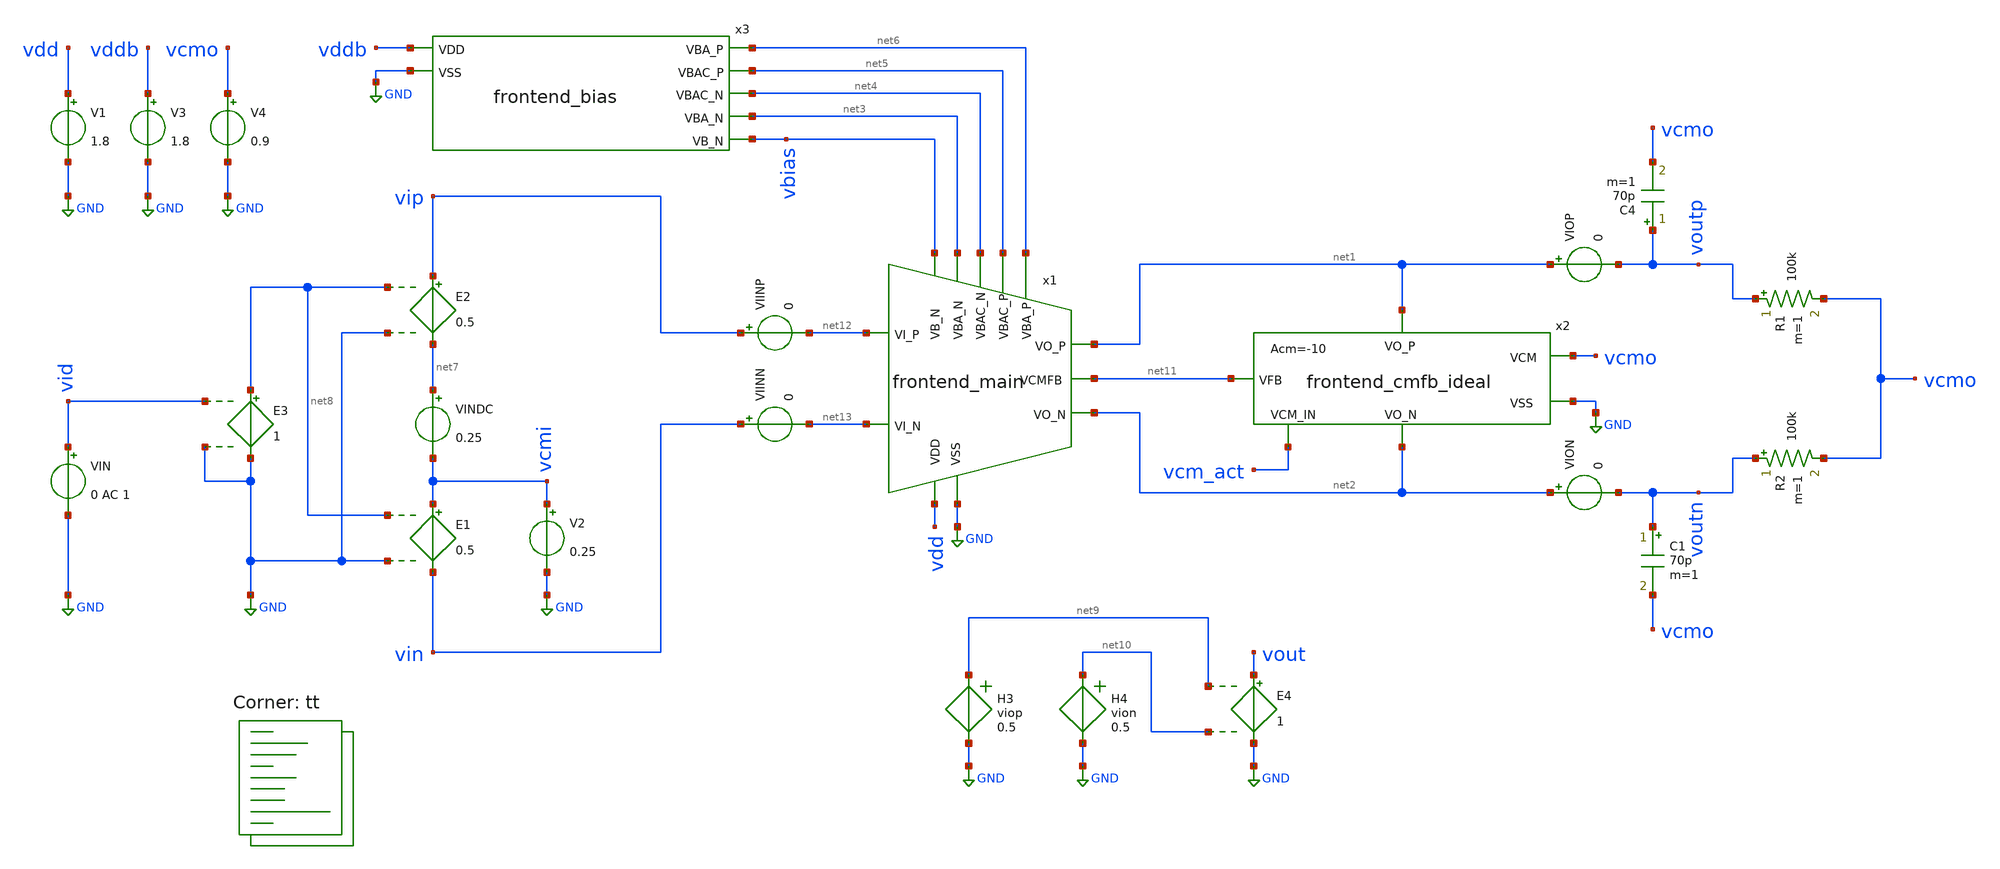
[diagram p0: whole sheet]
** sch_path: circuit-level/xschem/frontend/frontend_tb_int.sch
**.subckt frontend_tb_int
V1 vdd GND 1.8
V2 vcmi GND 0.25
E1 vcmi vin net8 GND 0.5
E2 vip net7 net8 GND 0.5
VIN vid GND 0 AC 1
VINDC net7 vcmi 0.25
x3 vddb net6 net5 net4 net3 vbias GND frontend_bias
V3 vddb GND 1.8
V4 vcmo GND 0.9
E3 net8 GND vid GND 1
VIOP net1 voutp 0
VION net2 voutn 0
H3 net9 GND viop 0.5
H4 net10 GND vion 0.5
E4 vout GND net9 net10 1
C1 voutn vcmo 70p m=1
R1 voutp vcmo 100k m=1
R2 voutn vcmo 100k m=1
C4 voutp vcmo 70p m=1
x1 vdd net11 net3 net4 net5 net6 net1 net2 net12 net13 vbias GND frontend_main
x2 net1 net2 net11 vcmo GND vcm_act frontend_cmfb_ideal ACM=-10
VIINP vip net12 0
VIINN vin net13 0
**** begin user architecture code
.lib $::SKYWATER_MODELS/sky130.lib.spice tt


.options savecurrents
.control
save all

let f_sig = 32
let f_min = 0.01
let f_max = 128
let tper_sig = 1/f_sig
let tfr_sig = tper_sig/2
alter @VIN[SIN] = [ 0 0.01 $&f_sig 0 0 0 ]
alter @VIN[DC] = 0.0

let tstep = 0.01/f_sig
let tstop = 500/f_sig
let tstart = 2500*tstep

set fnac = /foss/designs/frontend/frontend_int_ac.txt
set fntran = /foss/designs/frontend/frontend_int_tran.txt
set fnspec = /foss/designs/frontend/frontend_int_spec.txt
set fnhd = /foss/designs/frontend/frontend_int_hd.txt
set wr_singlescale
set wr_vecnames
option numdgt=5


** Main Simulations
	alter @VINDC[DC] = 0
	*dc VIN -500m 500m 31m
	ac dec 1000 0.1 1e7
	*alter @VINDC[DC] = 0.25
	tran $&tstep $&tstop $&tstart
	alter @VINDC[DC] = 0
	*noise v(vout) VIN dec 100 0.1 100k 1
	*noise v(vout) VIN dec 10 0.1 128

	*setplot noise1
	*let acgain = onoise_spectrum/inoise_spectrum

	*let m1a_in = onoise.m.xm1a.msky130_fd_pr__nfet_01v8/acgain
	*let m1b_in = onoise.m.xm1b.msky130_fd_pr__nfet_01v8/acgain

	*let m2a_in = onoise.m.xm2a.msky130_fd_pr__pfet_01v8_lvt/acgain
	*let m2b_in = onoise.m.xm2b.msky130_fd_pr__pfet_01v8_lvt/acgain

	*let m3a_in = onoise.m.xm3a.msky130_fd_pr__nfet_01v8/acgain
	*let m3b_in = onoise.m.xm3b.msky130_fd_pr__nfet_01v8/acgain

	*let rs_in = sqrt(onoise_rs1^2+onoise_rs2^2)/acgain

	*plot inoise_spectrum m1a_in m2a_in m3a_in rs_in

	*plot m2a_in m2b_in

	setplot ac1
	let vc = v(voutp)-v(voutn)
	let iod = (viop#branch-vion#branch)
	let ioc = @c1[i]
	let A = v(vc)/v(vin)
	let Gm = iod/v(vin)
	let Gm_c = ioc/v(vin)
	plot vdb(A) 180/PI*cphase(A)
	plot vdb(Gm)

	let i_in_p = viinp#branch
	let i_in_n = viinn#branch
	let zin = abs((v(vip)-v(vin))/((i_in_p-i_in_n)))

	plot vdb(zin)

	setplot tran1
	let vid = v(vid)
	let iod = (viop#branch-vion#branch)
	let vout = v(voutp)-v(voutn)
	let ioc = @c1[i]
	meas tran iod_max max iod
	meas tran ioc_max max ioc
	meas tran vid_max max vid
	let gm = iod_max/vid_max
	let gm_c = ioc_max/vid_max
	plot vid vout
	plot iod ioc


	plot gm gm_c
	wrdata $fntran iod

	** FFT

	linearize vout
	set specwindow=hanning
	fft vout
	setplot sp2

	let N = length(vout)
	let fres = frequency[n-1]/n
	let fmin_idx = ceil(const.f_min/fres)
	let fmax_idx = ceil(const.f_max/fres)

	let iod_spec = mag(vout)
	let iod_spec_slice = iod_spec[fmin_idx,fmax_idx]
	let freq = frequency[fmin_idx,fmax_idx]
	meas sp iod_max max iod_spec_slice
	let iod_spec_db = 20*log10(iod_spec_slice/iod_max)
	plot iod_spec_db vs freq

	** Calc HD2, HD3
	let sig_idx = ceil(const.f_sig/fres)
	let hd2_idx = 2*sig_idx
	let hd3_idx = 3*sig_idx
	let sig_pwr = iod_spec[sig_idx-1]^2+iod_spec[sig_idx]^2+iod_spec[sig_idx+1]^2
	let hd2_pwr = iod_spec[hd2_idx-1]^2+iod_spec[hd2_idx]^2+iod_spec[hd2_idx+1]^2
	let hd3_pwr = iod_spec[hd3_idx-1]^2+iod_spec[hd3_idx]^2+iod_spec[hd3_idx+1]^2
	let hd2 = sqrt(hd2_pwr/sig_pwr)
	let hd3 = sqrt(hd3_pwr/sig_pwr)
	let hd2_dB = 20*log10(hd2)
	let hd3_dB = 20*log10(hd3)
	setscale freq
	wrdata $fnspec iod_spec_db
	*wrdata $fnhd hd3[0] hd3_db[0] hd2[0] hd2_db[0] fres n

alter @VIN[DC] = 0
op
remzerovec
write frontend_tb_dc.raw
.endc

**** end user architecture code
**.ends
.GLOBAL GND
.end
